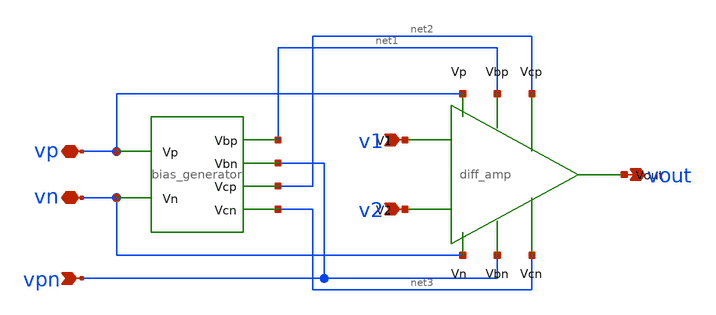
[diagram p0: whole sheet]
** sch_path: mini_proj_3/schematic/diffamp.sch
**.subckt diffamp v1 v2 vout vpn vp vn
*.ipin v1
*.ipin v2
*.opin vout
*.ipin vpn
*.iopin vp
*.iopin vn
X1 vp vn net1 vpn net2 net3 bias_generator
X2 vp vn net1 vpn net2 net3 v1 v2 vout diff_amp
**.ends
.end
